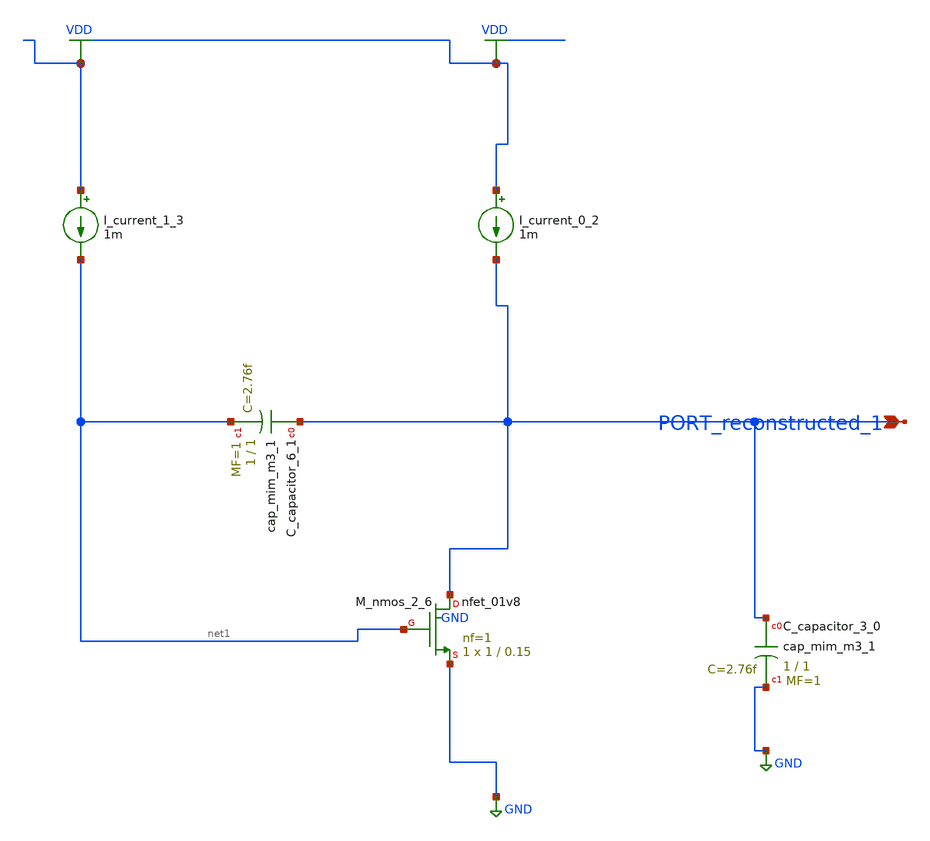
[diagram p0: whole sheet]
** sch_path: schematics/AMSNet/732.sch
**.subckt 732 PORT_reconstructed_1
*.ipin PORT_reconstructed_1
XC_capacitor_3_0 PORT_reconstructed_1 GND sky130_fd_pr__cap_mim_m3_1 W=1 L=1 MF=1 m=1
XC_capacitor_6_1 PORT_reconstructed_1 net1 sky130_fd_pr__cap_mim_m3_1 W=1 L=1 MF=1 m=1
I_current_0_2 VDD PORT_reconstructed_1 1m
I_current_1_3 VDD net1 1m
XM_nmos_2_6 PORT_reconstructed_1 net1 GND GND sky130_fd_pr__nfet_01v8 L=0.15 W=1 nf=1 ad='int((1 + 1)/2) * 1 / 1 * 0.29'
+ as='int((1 + 2)/2) * 1 / 1 * 0.29' pd='2*int((1 + 1)/2) * (1 / 1 + 0.29)' ps='2*int((1 + 2)/2) * (1 / 1 + 0.29)'
+ nrd='0.29 / 1 ' nrs='0.29 / 1 ' sa=0 sb=0 sd=0 mult=1 m=1
**.ends
.GLOBAL GND
.GLOBAL VDD
.end
